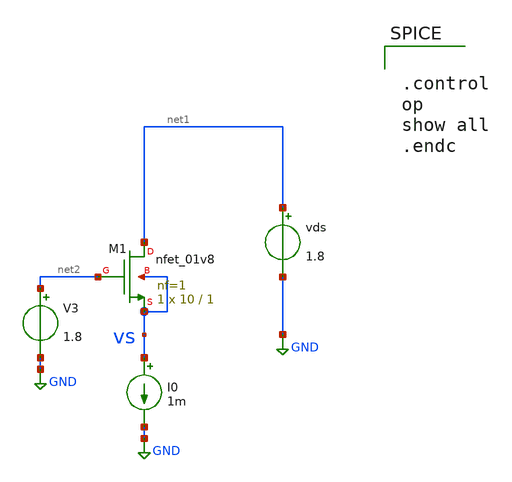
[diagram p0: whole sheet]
** sch_path: mos_sizing/mos_modelcheck.sch
**.subckt mos_modelcheck
XM1 net1 net2 vs vs sky130_fd_pr__nfet_01v8 L=1 W=10 nf=1 ad='int((nf+1)/2) * W/nf * 0.29' as='int((nf+2)/2) * W/nf * 0.29'
+ pd='2*int((nf+1)/2) * (W/nf + 0.29)' ps='2*int((nf+2)/2) * (W/nf + 0.29)' nrd='0.29 / W' nrs='0.29 / W'
+ sa=0 sb=0 sd=0 mult=1 m=1
vds net1 GND 1.8
V3 net2 GND 1.8
I0 vs GND 1m
**** begin user architecture code


.option wnflag = 1
.lib /usr/local/share/pdk/sky130A/libs.tech/ngspice/sky130.lib.spice tt
.include /usr/local/share/pdk/sky130A/libs.ref/sky130_fd_pr/spice/sky130_fd_pr__ind_05_220.model.spice
.param mc_mm_switch=0




.control
op
show all
.endc


**** end user architecture code
**.ends
.GLOBAL GND
.end
